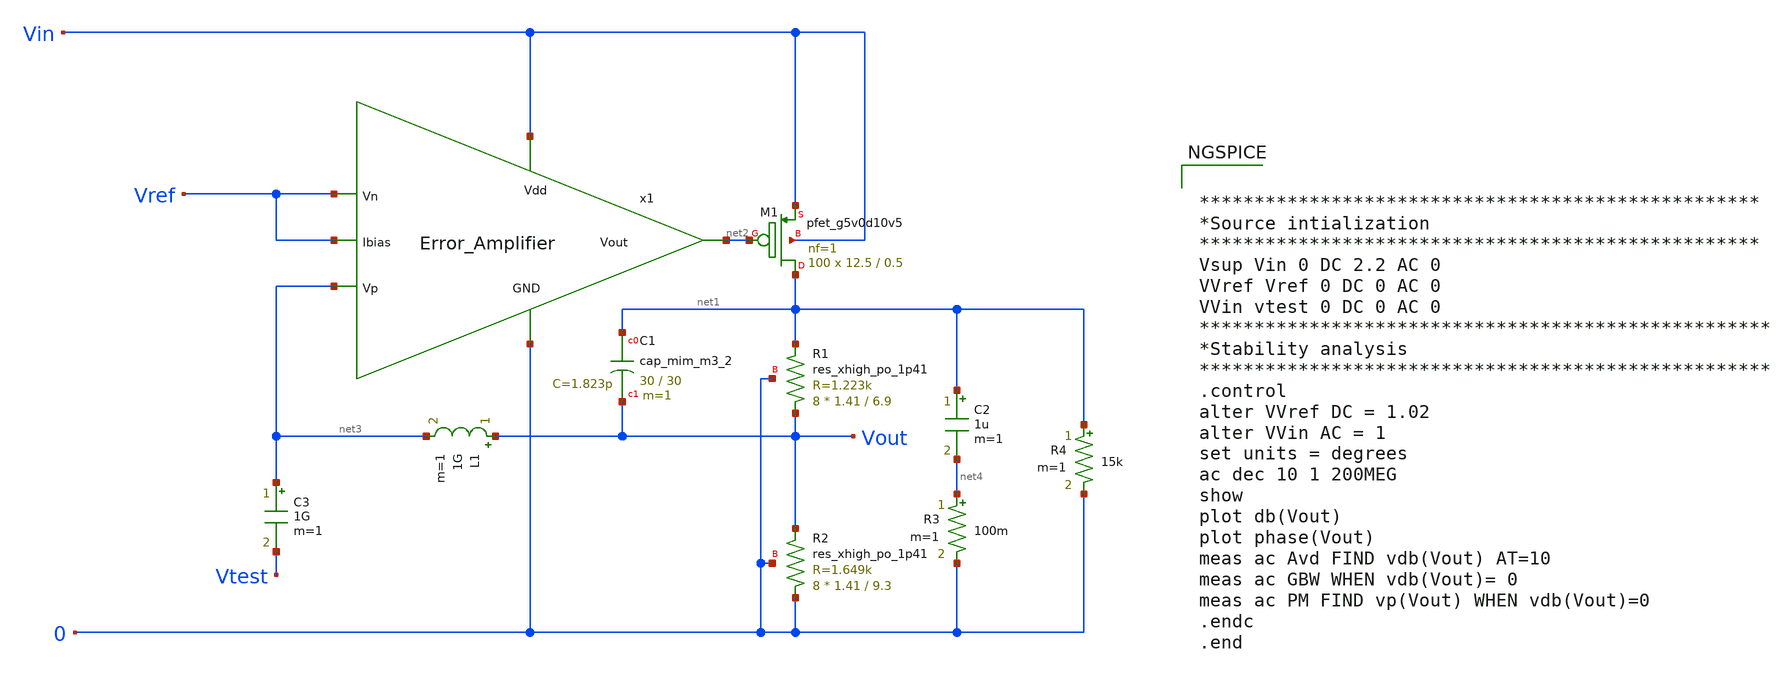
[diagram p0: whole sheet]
** sch_path: Analog_Blocks/LDO/Testbench/LDO_Miller_1.8v_meas_STB.sch
**.subckt LDO_Miller_1.8v_meas_STB
XC1 net1 Vout sky130_fd_pr__cap_mim_m3_2 W=30 L=30 MF=1 m=1
XM1 net1 net2 Vin Vin sky130_fd_pr__pfet_g5v0d10v5 L=0.5 W=12.5 nf=1 ad='int((nf+1)/2) * W/nf * 0.29'
+ as='int((nf+2)/2) * W/nf * 0.29' pd='2*int((nf+1)/2) * (W/nf + 0.29)' ps='2*int((nf+2)/2) * (W/nf + 0.29)'
+ nrd='0.29 / W' nrs='0.29 / W' sa=0 sb=0 sd=0 mult=100 m=100
x1 Vin Vref net3 net2 Vref 0 Error_Amplifier
XR1 Vout net1 0 sky130_fd_pr__res_xhigh_po_1p41 L=6.9 mult=8 m=8
XR2 0 Vout 0 sky130_fd_pr__res_xhigh_po_1p41 L=9.3 mult=8 m=8
C2 net1 net4 1u m=1
R3 net4 0 100m m=1
L1 Vout net3 1G m=1
C3 net3 Vtest 1G m=1
R4 net1 0 15k m=1
**** begin user architecture code


***************************************************
*Source intialization
***************************************************
Vsup Vin 0 DC 2.2 AC 0
VVref Vref 0 DC 0 AC 0
VVin vtest 0 DC 0 AC 0
****************************************************
*Stability analysis
****************************************************
.control
alter VVref DC = 1.02
alter VVin AC = 1
set units = degrees
ac dec 10 1 200MEG
show
plot db(Vout)
plot phase(Vout)
meas ac Avd FIND vdb(Vout) AT=10
meas ac GBW WHEN vdb(Vout)= 0
meas ac PM FIND vp(Vout) WHEN vdb(Vout)=0
.endc
.end



.include ~/Analog_blocks/models/skywater-pdk/libraries/sky130_fd_pr/latest/cells/nfet_01v8/sky130_fd_pr__nfet_01v8__tt.corner.spice
.include ~/Analog_blocks/models/skywater-pdk/libraries/sky130_fd_pr/latest/cells/nfet_01v8_lvt/sky130_fd_pr__nfet_01v8_lvt__tt.corner.spice
.include ~/Analog_blocks/models/skywater-pdk/libraries/sky130_fd_pr/latest/cells/pfet_01v8/sky130_fd_pr__pfet_01v8__tt.corner.spice
.include ~/Analog_blocks/models/skywater-pdk/libraries/sky130_fd_pr/latest/cells/nfet_03v3_nvt/sky130_fd_pr__nfet_03v3_nvt__tt.corner.spice
.include ~/Analog_blocks/models/skywater-pdk/libraries/sky130_fd_pr/latest/cells/nfet_05v0_nvt/sky130_fd_pr__nfet_05v0_nvt__tt.corner.spice
.include ~/Analog_blocks/models/skywater-pdk/libraries/sky130_fd_pr/latest/cells/esd_nfet_01v8/sky130_fd_pr__esd_nfet_01v8__tt.corner.spice
.include ~/Analog_blocks/models/skywater-pdk/libraries/sky130_fd_pr/latest/cells/pfet_01v8_lvt/sky130_fd_pr__pfet_01v8_lvt__tt.corner.spice
.include ~/Analog_blocks/models/skywater-pdk/libraries/sky130_fd_pr/latest/cells/pfet_01v8_hvt/sky130_fd_pr__pfet_01v8_hvt__tt.corner.spice
.include ~/Analog_blocks/models/skywater-pdk/libraries/sky130_fd_pr/latest/cells/esd_pfet_g5v0d10v5/sky130_fd_pr__esd_pfet_g5v0d10v5__tt.corner.spice
.include ~/Analog_blocks/models/skywater-pdk/libraries/sky130_fd_pr/latest/cells/pfet_g5v0d10v5/sky130_fd_pr__pfet_g5v0d10v5__tt.corner.spice
.include ~/Analog_blocks/models/skywater-pdk/libraries/sky130_fd_pr/latest/cells/pfet_g5v0d16v0/sky130_fd_pr__pfet_g5v0d16v0__tt.corner.spice
.include ~/Analog_blocks/models/skywater-pdk/libraries/sky130_fd_pr/latest/cells/nfet_g5v0d10v5/sky130_fd_pr__nfet_g5v0d10v5__tt.corner.spice
.include ~/Analog_blocks/models/skywater-pdk/libraries/sky130_fd_pr/latest/cells/nfet_g5v0d16v0/sky130_fd_pr__nfet_g5v0d16v0__tt_discrete.corner.spice
.include ~/Analog_blocks/models/skywater-pdk/libraries/sky130_fd_pr/latest/cells/esd_nfet_g5v0d10v5/sky130_fd_pr__esd_nfet_g5v0d10v5__tt.corner.spice
.include ~/Analog_blocks/models/skywater-pdk/libraries/sky130_fd_pr/latest/models/corners/tt/nonfet.spice
* Mismatch parameters
.include ~/Analog_blocks/models/skywater-pdk/libraries/sky130_fd_pr/latest/cells/nfet_01v8/sky130_fd_pr__nfet_01v8__mismatch.corner.spice
.include ~/Analog_blocks/models/skywater-pdk/libraries/sky130_fd_pr/latest/cells/pfet_01v8/sky130_fd_pr__pfet_01v8__mismatch.corner.spice
.include ~/Analog_blocks/models/skywater-pdk/libraries/sky130_fd_pr/latest/cells/nfet_01v8_lvt/sky130_fd_pr__nfet_01v8_lvt__mismatch.corner.spice
.include ~/Analog_blocks/models/skywater-pdk/libraries/sky130_fd_pr/latest/cells/pfet_01v8_lvt/sky130_fd_pr__pfet_01v8_lvt__mismatch.corner.spice
.include ~/Analog_blocks/models/skywater-pdk/libraries/sky130_fd_pr/latest/cells/pfet_01v8_hvt/sky130_fd_pr__pfet_01v8_hvt__mismatch.corner.spice
.include ~/Analog_blocks/models/skywater-pdk/libraries/sky130_fd_pr/latest/cells/nfet_g5v0d10v5/sky130_fd_pr__nfet_g5v0d10v5__mismatch.corner.spice
.include ~/Analog_blocks/models/skywater-pdk/libraries/sky130_fd_pr/latest/cells/pfet_g5v0d10v5/sky130_fd_pr__pfet_g5v0d10v5__mismatch.corner.spice
.include ~/Analog_blocks/models/skywater-pdk/libraries/sky130_fd_pr/latest/cells/nfet_05v0_nvt/sky130_fd_pr__nfet_05v0_nvt__mismatch.corner.spice
.include ~/Analog_blocks/models/skywater-pdk/libraries/sky130_fd_pr/latest/cells/nfet_03v3_nvt/sky130_fd_pr__nfet_03v3_nvt__mismatch.corner.spice
* Resistor
.include ~/Analog_blocks/models/skywater-pdk/libraries/sky130_fd_pr/latest/models/r+c/res_typical__cap_typical.spice
.include ~/Analog_blocks/models/skywater-pdk/libraries/sky130_fd_pr/latest/models/r+c/res_typical__cap_typical__lin.spice
* Special cells
.include ~/Analog_blocks/models/skywater-pdk/libraries/sky130_fd_pr/latest/models/corners/tt/specialized_cells.spice
* All models
.include ~/Analog_blocks/models/skywater-pdk/libraries/sky130_fd_pr/latest/models/all.spice
* Corner
.include ~/Analog_blocks/models/skywater-pdk/libraries/sky130_fd_pr/latest/models/corners/tt/rf.spice

**** end user architecture code
**.ends
.end
